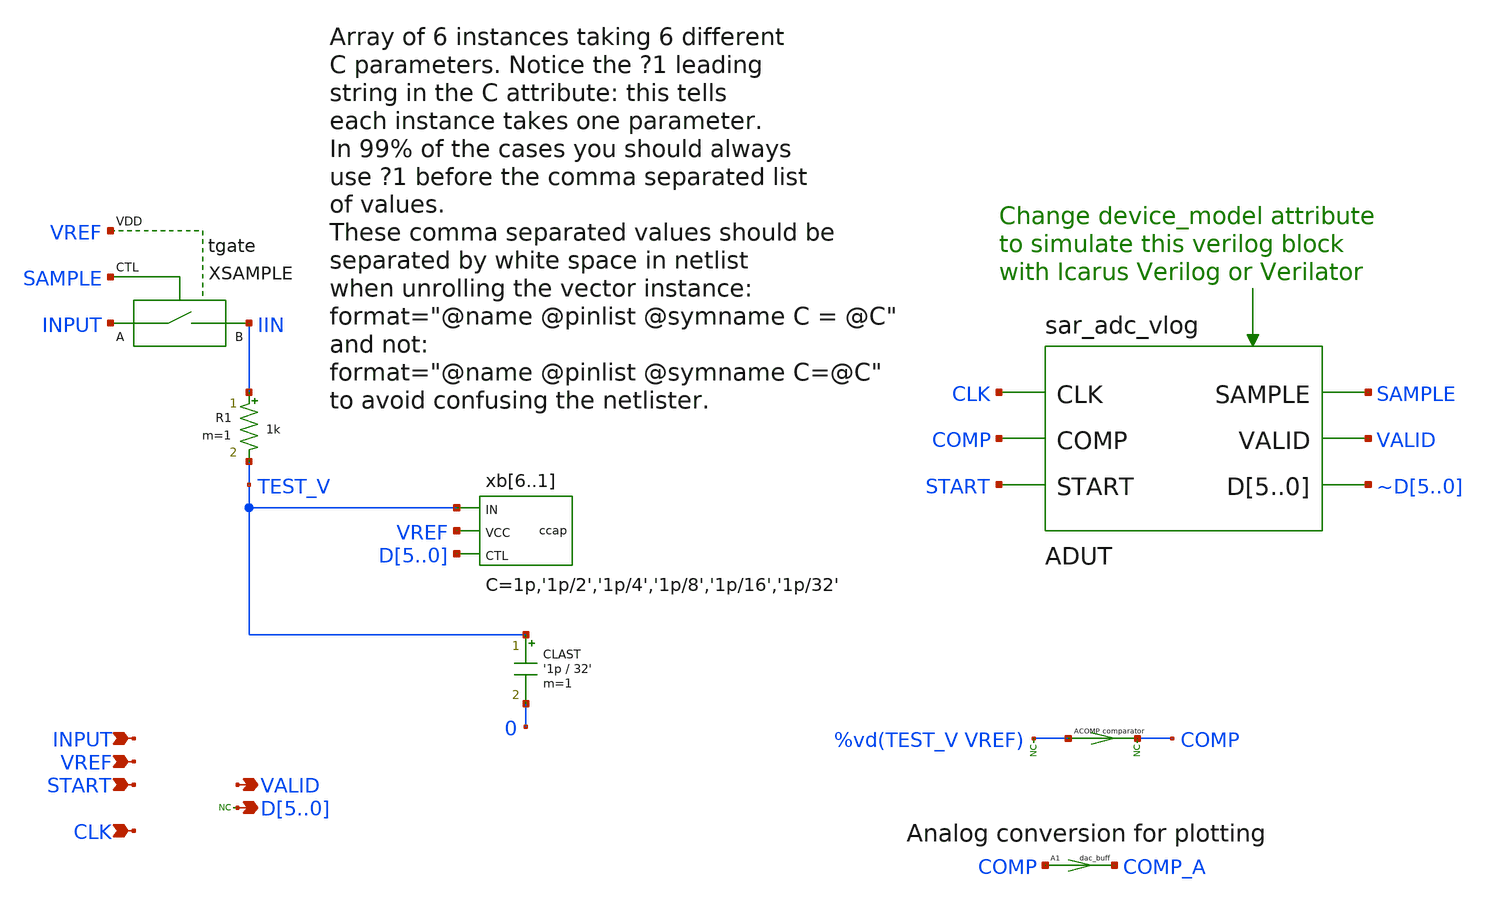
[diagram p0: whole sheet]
** sch_path: xschem_libs_newsym/ngspice_verilog_cosim/sar_adc/schematic/sar_adc.sch
**.subckt sar_adc INPUT VREF START VALID CLK D5,D4,D3,D2,D1,D0
*.ipin INPUT
*.ipin VREF
*.ipin START
*.opin VALID
*.ipin CLK
*.opin D5,D4,D3,D2,D1,D0
CLAST TEST_V 0 '1p / 32' m=1
ACOMP [ %vd(TEST_V VREF) ] [ COMP ] comparator
XSAMPLE INPUT IIN SAMPLE VREF tgate
R1 IIN TEST_V 1k m=1
ADUT [ CLK COMP START ] [ SAMPLE VALID ~D5 ~D4 ~D3 ~D2 ~D1 ~D0 ] dut
A1 [ COMP ] [ COMP_A ] dac_buff
* noconn D[5..0]
* noconn COMP
* noconn %vd(TEST_V VREF)
xb6 TEST_V VREF D5 ccap C=1p,'1p/2','1p/4','1p/8','1p/16','1p/32'
xb5 TEST_V VREF D4 ccap C=1p,'1p/2','1p/4','1p/8','1p/16','1p/32'
xb4 TEST_V VREF D3 ccap C=1p,'1p/2','1p/4','1p/8','1p/16','1p/32'
xb3 TEST_V VREF D2 ccap C=1p,'1p/2','1p/4','1p/8','1p/16','1p/32'
xb2 TEST_V VREF D1 ccap C=1p,'1p/2','1p/4','1p/8','1p/16','1p/32'
xb1 TEST_V VREF D0 ccap C=1p,'1p/2','1p/4','1p/8','1p/16','1p/32'
**.ends
**** begin user architecture code
.model dut d_cosim simulation="ivlng" sim_args=["adc"]
.model comparator adc_bridge in_low=0 in_high=0
.model dac_buff dac_bridge input_load=1e-15 t_rise=10n t_fall=10n  out_low=0 out_high=3.3
**** end user architecture code
.end
